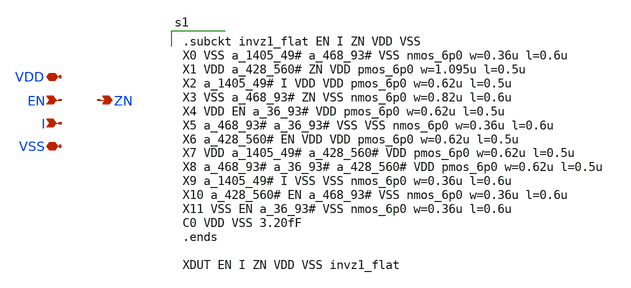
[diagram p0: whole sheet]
** sch_path: xschem/invz1.sch
**.subckt invz1 EN I ZN VDD VSS
*.ipin EN
*.ipin I
*.opin ZN
*.iopin VDD
*.iopin VSS
**** begin user architecture code

.subckt invz1_flat EN I ZN VDD VSS
X0 VSS a_1405_49# a_468_93# VSS nmos_6p0 w=0.36u l=0.6u
X1 VDD a_428_560# ZN VDD pmos_6p0 w=1.095u l=0.5u
X2 a_1405_49# I VDD VDD pmos_6p0 w=0.62u l=0.5u
X3 VSS a_468_93# ZN VSS nmos_6p0 w=0.82u l=0.6u
X4 VDD EN a_36_93# VDD pmos_6p0 w=0.62u l=0.5u
X5 a_468_93# a_36_93# VSS VSS nmos_6p0 w=0.36u l=0.6u
X6 a_428_560# EN VDD VDD pmos_6p0 w=0.62u l=0.5u
X7 VDD a_1405_49# a_428_560# VDD pmos_6p0 w=0.62u l=0.5u
X8 a_468_93# a_36_93# a_428_560# VDD pmos_6p0 w=0.62u l=0.5u
X9 a_1405_49# I VSS VSS nmos_6p0 w=0.36u l=0.6u
X10 a_428_560# EN a_468_93# VSS nmos_6p0 w=0.36u l=0.6u
X11 VSS EN a_36_93# VSS nmos_6p0 w=0.36u l=0.6u
C0 VDD VSS 3.20fF
.ends

XDUT EN I ZN VDD VSS invz1_flat


**** end user architecture code
**.ends
.end
